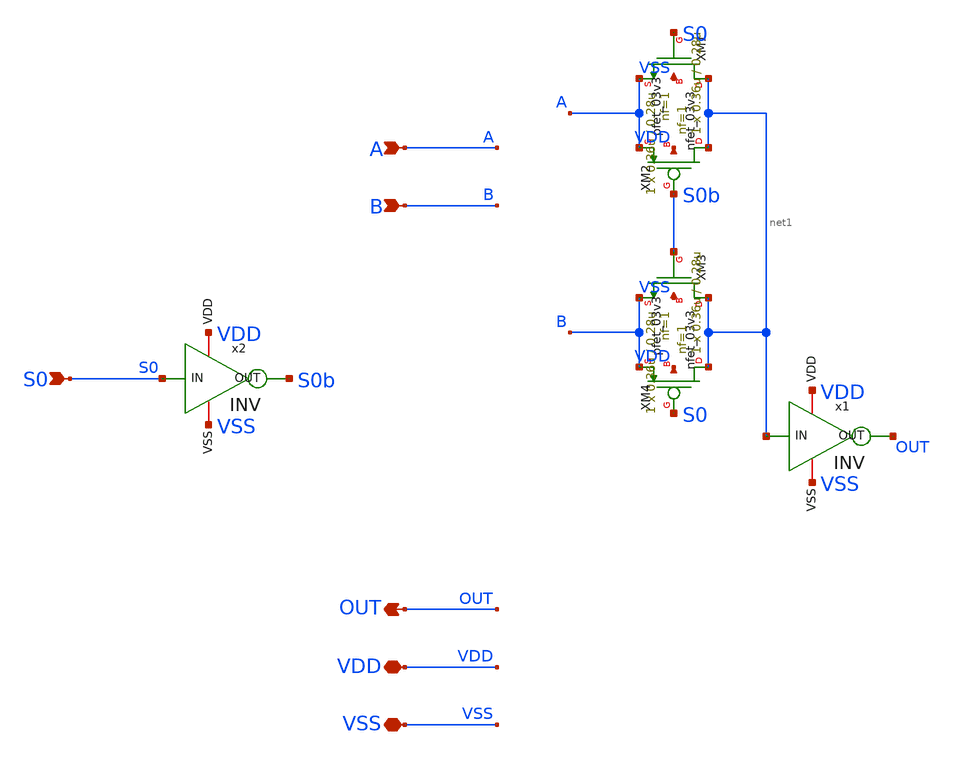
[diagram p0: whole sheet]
** sch_path: CAD4/2:1_mux.sch
**.subckt 2:1_mux A B S0 OUT VDD VSS
*.ipin A
*.ipin B
*.ipin S0
*.opin OUT
*.iopin VDD
*.iopin VSS
XM1 net1 S0 A VSS nfet_03v3 L=0.28u W=0.36u nf=1 ad='int((nf+1)/2) * W/nf * 0.18u' as='int((nf+2)/2) * W/nf * 0.18u'
+ pd='2*int((nf+1)/2) * (W/nf + 0.18u)' ps='2*int((nf+2)/2) * (W/nf + 0.18u)' nrd='0.18u / W' nrs='0.18u / W'
+ sa=0 sb=0 sd=0 m=1
XM2 net1 S0b A VDD pfet_03v3 L=0.28u W=0.36u nf=1 ad='int((nf+1)/2) * W/nf * 0.18u' as='int((nf+2)/2) * W/nf * 0.18u'
+ pd='2*int((nf+1)/2) * (W/nf + 0.18u)' ps='2*int((nf+2)/2) * (W/nf + 0.18u)' nrd='0.18u / W' nrs='0.18u / W'
+ sa=0 sb=0 sd=0 m=1
XM3 net1 S0b B VSS nfet_03v3 L=0.28u W=0.36u nf=1 ad='int((nf+1)/2) * W/nf * 0.18u' as='int((nf+2)/2) * W/nf * 0.18u'
+ pd='2*int((nf+1)/2) * (W/nf + 0.18u)' ps='2*int((nf+2)/2) * (W/nf + 0.18u)' nrd='0.18u / W' nrs='0.18u / W'
+ sa=0 sb=0 sd=0 m=1
XM4 net1 S0 B VDD pfet_03v3 L=0.28u W=0.36u nf=1 ad='int((nf+1)/2) * W/nf * 0.18u' as='int((nf+2)/2) * W/nf * 0.18u'
+ pd='2*int((nf+1)/2) * (W/nf + 0.18u)' ps='2*int((nf+2)/2) * (W/nf + 0.18u)' nrd='0.18u / W' nrs='0.18u / W'
+ sa=0 sb=0 sd=0 m=1
x1 VDD net1 OUT VSS INV
x2 VDD S0 S0b VSS INV
**.ends
.end
